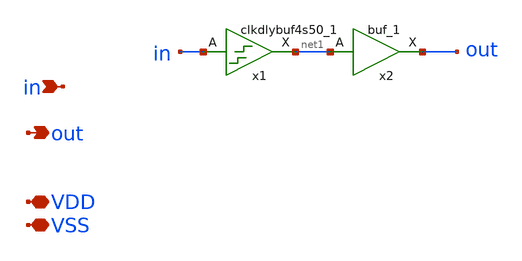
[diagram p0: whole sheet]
** sch_path: xschem/src/prop_delay_block/prop_delay_block.sch
**.subckt prop_delay_block in out VDD VSS
*.ipin in
*.opin out
*.iopin VDD
*.iopin VSS
x1 in VSS VSS VDD VDD net1 sky130_fd_sc_hd__clkdlybuf4s50_1
x2 net1 VSS VSS VDD VDD out sky130_fd_sc_hd__buf_1
**.ends
.end
